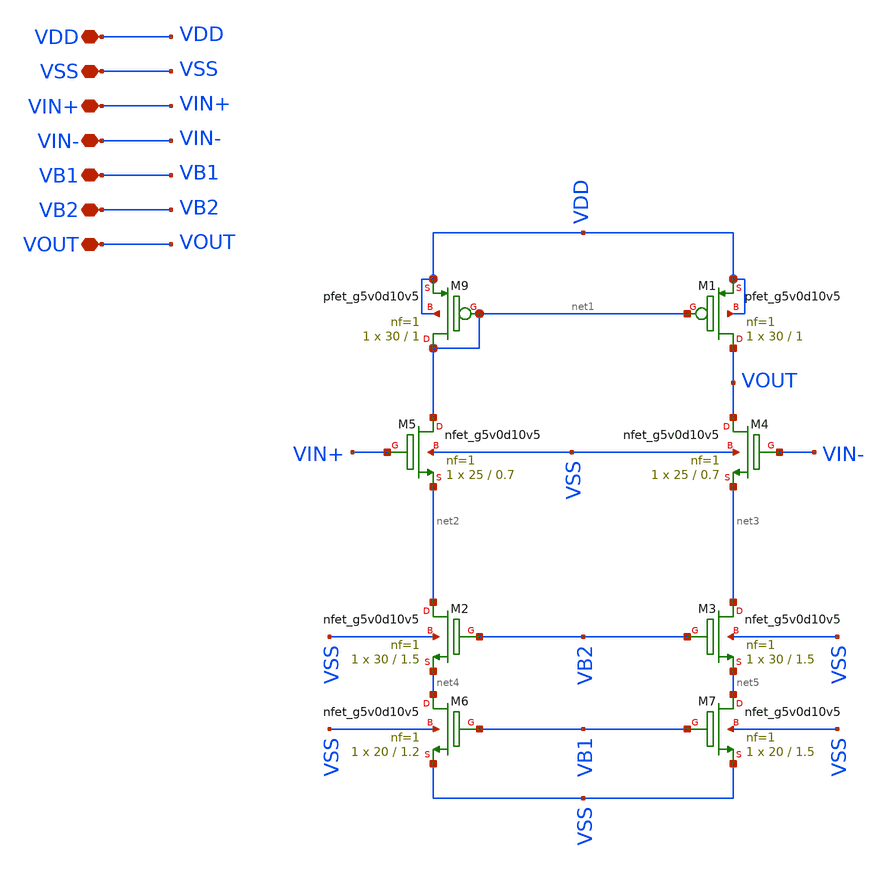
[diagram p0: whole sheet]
** sch_path: old stuff/folded_cascode_amplifier_upgraded/cmfb_amp/cmfb_amp.sch
**.subckt cmfb_amp VDD VSS VIN+ VIN- VB1 VB2 VOUT
*.iopin VDD
*.iopin VSS
*.iopin VIN+
*.iopin VIN-
*.iopin VB1
*.iopin VB2
*.iopin VOUT
XM9 net1 net1 VDD VDD sky130_fd_pr__pfet_g5v0d10v5 L=1 W=30 nf=1 ad='int((1 + 1)/2) * 30 / 1 * 0.29'
+ as='int((1 + 2)/2) * 30 / 1 * 0.29' pd='2*int((1 + 1)/2) * (30 / 1 + 0.29)' ps='2*int((1 + 2)/2) * (30 / 1 + 0.29)'
+ nrd='0.29 / 30 ' nrs='0.29 / 30 ' sa=0 sb=0 sd=0 mult=1 m=1
XM1 VOUT net1 VDD VDD sky130_fd_pr__pfet_g5v0d10v5 L=1 W=30 nf=1 ad='int((1 + 1)/2) * 30 / 1 * 0.29'
+ as='int((1 + 2)/2) * 30 / 1 * 0.29' pd='2*int((1 + 1)/2) * (30 / 1 + 0.29)' ps='2*int((1 + 2)/2) * (30 / 1 + 0.29)'
+ nrd='0.29 / 30 ' nrs='0.29 / 30 ' sa=0 sb=0 sd=0 mult=1 m=1
XM5 net1 VIN+ net2 VSS sky130_fd_pr__nfet_g5v0d10v5 L=0.7 W=25 nf=1 ad='int((1 + 1)/2) * 25 / 1 * 0.29'
+ as='int((1 + 2)/2) * 25 / 1 * 0.29' pd='2*int((1 + 1)/2) * (25 / 1 + 0.29)' ps='2*int((1 + 2)/2) * (25 / 1 + 0.29)'
+ nrd='0.29 / 25 ' nrs='0.29 / 25 ' sa=0 sb=0 sd=0 mult=1 m=1
XM4 VOUT VIN- net3 VSS sky130_fd_pr__nfet_g5v0d10v5 L=0.7 W=25 nf=1 ad='int((1 + 1)/2) * 25 / 1 * 0.29'
+ as='int((1 + 2)/2) * 25 / 1 * 0.29' pd='2*int((1 + 1)/2) * (25 / 1 + 0.29)' ps='2*int((1 + 2)/2) * (25 / 1 + 0.29)'
+ nrd='0.29 / 25 ' nrs='0.29 / 25 ' sa=0 sb=0 sd=0 mult=1 m=1
XM2 net2 VB2 net4 VSS sky130_fd_pr__nfet_g5v0d10v5 L=1.5 W=30 nf=1 ad='int((1 + 1)/2) * 30 / 1 * 0.29'
+ as='int((1 + 2)/2) * 30 / 1 * 0.29' pd='2*int((1 + 1)/2) * (30 / 1 + 0.29)' ps='2*int((1 + 2)/2) * (30 / 1 + 0.29)'
+ nrd='0.29 / 30 ' nrs='0.29 / 30 ' sa=0 sb=0 sd=0 mult=1 m=1
XM6 net4 VB1 VSS VSS sky130_fd_pr__nfet_g5v0d10v5 L=1.2 W=20 nf=1 ad='int((1 + 1)/2) * 20 / 1 * 0.29'
+ as='int((1 + 2)/2) * 20 / 1 * 0.29' pd='2*int((1 + 1)/2) * (20 / 1 + 0.29)' ps='2*int((1 + 2)/2) * (20 / 1 + 0.29)'
+ nrd='0.29 / 20 ' nrs='0.29 / 20 ' sa=0 sb=0 sd=0 mult=1 m=1
XM7 net5 VB1 VSS VSS sky130_fd_pr__nfet_g5v0d10v5 L=1.5 W=20 nf=1 ad='int((1 + 1)/2) * 20 / 1 * 0.29'
+ as='int((1 + 2)/2) * 20 / 1 * 0.29' pd='2*int((1 + 1)/2) * (20 / 1 + 0.29)' ps='2*int((1 + 2)/2) * (20 / 1 + 0.29)'
+ nrd='0.29 / 20 ' nrs='0.29 / 20 ' sa=0 sb=0 sd=0 mult=1 m=1
XM3 net3 VB2 net5 VSS sky130_fd_pr__nfet_g5v0d10v5 L=1.5 W=30 nf=1 ad='int((1 + 1)/2) * 30 / 1 * 0.29'
+ as='int((1 + 2)/2) * 30 / 1 * 0.29' pd='2*int((1 + 1)/2) * (30 / 1 + 0.29)' ps='2*int((1 + 2)/2) * (30 / 1 + 0.29)'
+ nrd='0.29 / 30 ' nrs='0.29 / 30 ' sa=0 sb=0 sd=0 mult=1 m=1
**.ends
.end
